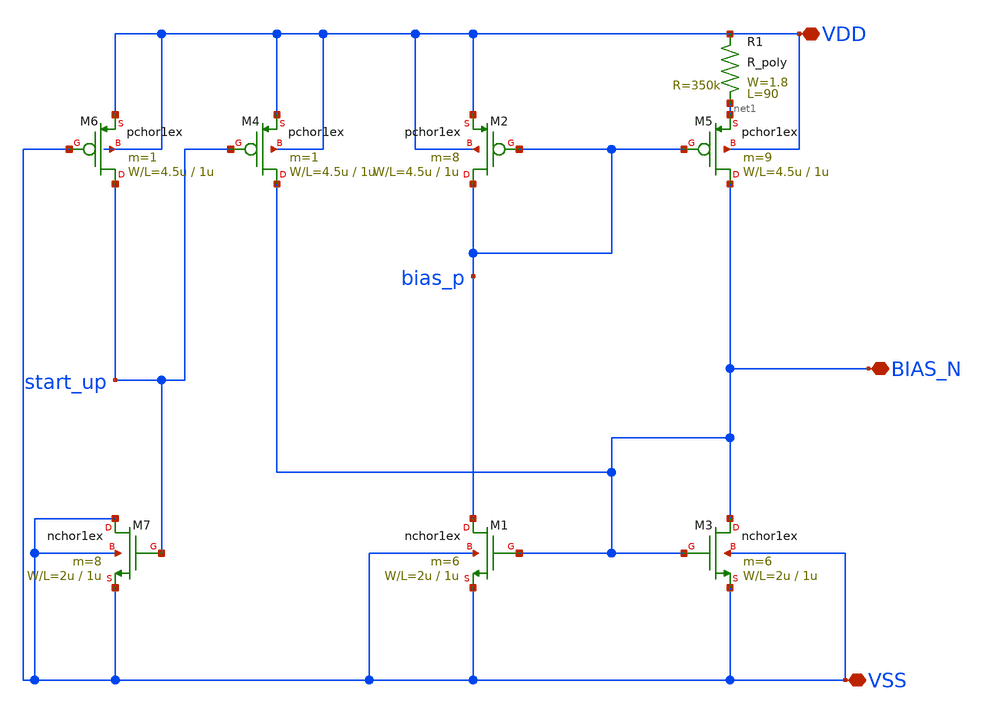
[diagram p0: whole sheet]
** sch_path: design/.design_bk/xschem/VCO/SA_DIV_CompBias.sch
**.subckt SA_DIV_CompBias VDD VSS BIAS_N
*.iopin VDD
*.iopin VSS
*.iopin BIAS_N
M3 BIAS_N BIAS_N VSS VSS nchor1ex L=1u W=2u m=6
M1 bias_p BIAS_N VSS VSS nchor1ex L=1u W=2u m=6
M5 BIAS_N bias_p net1 VDD pchor1ex L=1u W=4.5u m=9
M2 bias_p bias_p VDD VDD pchor1ex L=1u W=4.5u m=8
R1 net1 VDD R_poly W=1.8 L=90
M4 BIAS_N start_up VDD VDD pchor1ex L=1u W=4.5u m=1
M6 start_up VSS VDD VDD pchor1ex L=1u W=4.5u m=1
M7 VSS start_up VSS VSS nchor1ex L=1u W=2u m=8
**.ends
.end
